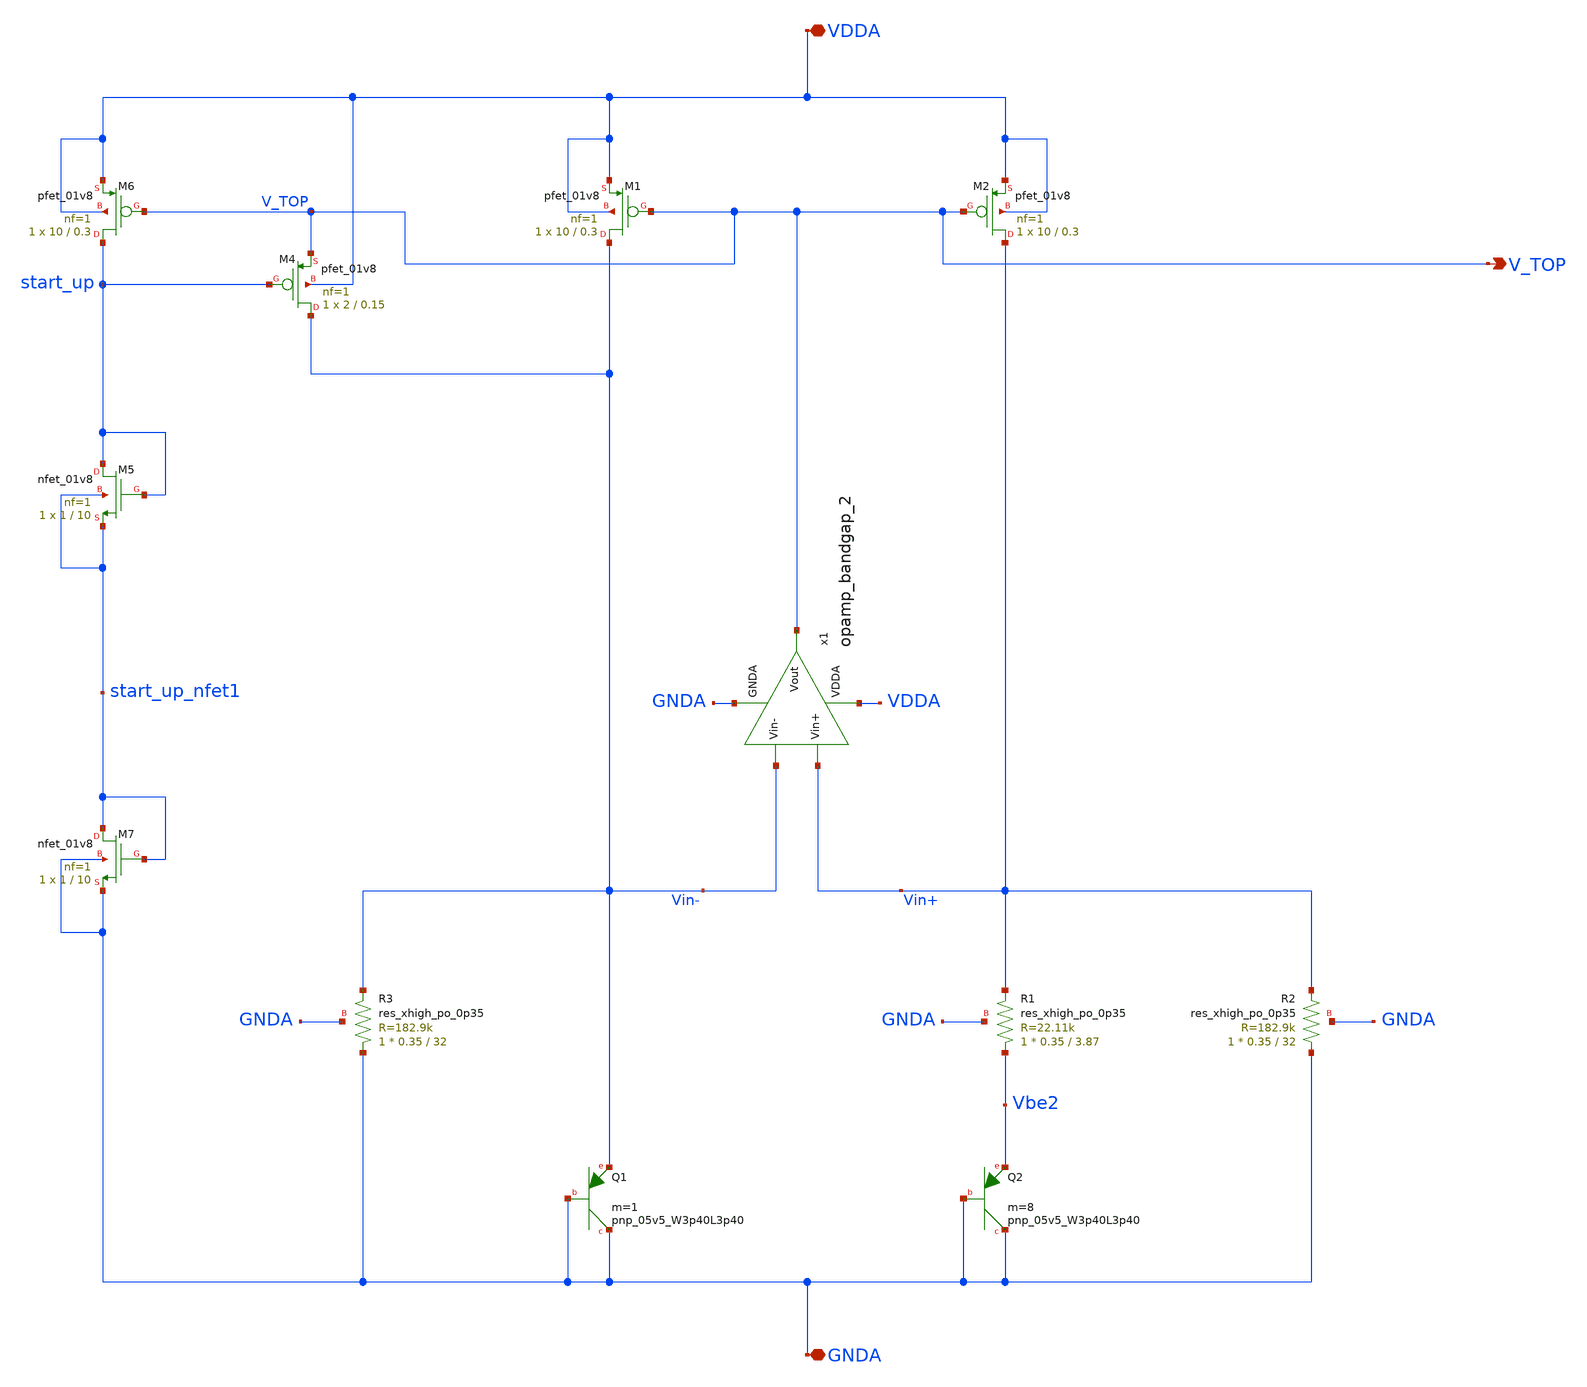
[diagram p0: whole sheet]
** sch_path: projects/bandgapref/xschem_ngspice/new_files/BGR_vtop_out.sch
**.subckt BGR_vtop_out VDDA GNDA V_TOP
*.iopin VDDA
*.iopin GNDA
*.opin V_TOP
XQ1 GNDA GNDA Vin- sky130_fd_pr__pnp_05v5_W3p40L3p40 m=1
XQ2 GNDA GNDA Vbe2 sky130_fd_pr__pnp_05v5_W3p40L3p40 m=8
XM1 Vin- V_TOP VDDA VDDA sky130_fd_pr__pfet_01v8 L=0.3 W=10 nf=1 ad='int((nf+1)/2) * W/nf * 0.29' as='int((nf+2)/2) * W/nf * 0.29'
+ pd='2*int((nf+1)/2) * (W/nf + 0.29)' ps='2*int((nf+2)/2) * (W/nf + 0.29)' nrd='0.29 / W' nrs='0.29 / W'
+ sa=0 sb=0 sd=0 mult=1 m=1
XM2 Vin+ V_TOP VDDA VDDA sky130_fd_pr__pfet_01v8 L=0.3 W=10 nf=1 ad='int((nf+1)/2) * W/nf * 0.29' as='int((nf+2)/2) * W/nf * 0.29'
+ pd='2*int((nf+1)/2) * (W/nf + 0.29)' ps='2*int((nf+2)/2) * (W/nf + 0.29)' nrd='0.29 / W' nrs='0.29 / W'
+ sa=0 sb=0 sd=0 mult=1 m=1
XR1 Vbe2 Vin+ GNDA sky130_fd_pr__res_xhigh_po_0p35 L=3.87 mult=1 m=1
XR2 GNDA Vin+ GNDA sky130_fd_pr__res_xhigh_po_0p35 L=32 mult=1 m=1
XR3 GNDA Vin- GNDA sky130_fd_pr__res_xhigh_po_0p35 L=32 mult=1 m=1
XM5 start_up start_up start_up_nfet1 start_up_nfet1 sky130_fd_pr__nfet_01v8 L=10 W=1 nf=1 ad='int((nf+1)/2) * W/nf * 0.29'
+ as='int((nf+2)/2) * W/nf * 0.29' pd='2*int((nf+1)/2) * (W/nf + 0.29)' ps='2*int((nf+2)/2) * (W/nf + 0.29)'
+ nrd='0.29 / W' nrs='0.29 / W' sa=0 sb=0 sd=0 mult=1 m=1
XM6 start_up V_TOP VDDA VDDA sky130_fd_pr__pfet_01v8 L=0.3 W=10 nf=1 ad='int((nf+1)/2) * W/nf * 0.29'
+ as='int((nf+2)/2) * W/nf * 0.29' pd='2*int((nf+1)/2) * (W/nf + 0.29)' ps='2*int((nf+2)/2) * (W/nf + 0.29)'
+ nrd='0.29 / W' nrs='0.29 / W' sa=0 sb=0 sd=0 mult=1 m=1
XM4 Vin- start_up V_TOP VDDA sky130_fd_pr__pfet_01v8 L=0.15 W=2 nf=1 ad='int((nf+1)/2) * W/nf * 0.29'
+ as='int((nf+2)/2) * W/nf * 0.29' pd='2*int((nf+1)/2) * (W/nf + 0.29)' ps='2*int((nf+2)/2) * (W/nf + 0.29)'
+ nrd='0.29 / W' nrs='0.29 / W' sa=0 sb=0 sd=0 mult=1 m=1
XM7 start_up_nfet1 start_up_nfet1 GNDA GNDA sky130_fd_pr__nfet_01v8 L=10 W=1 nf=1 ad='int((nf+1)/2) * W/nf * 0.29'
+ as='int((nf+2)/2) * W/nf * 0.29' pd='2*int((nf+1)/2) * (W/nf + 0.29)' ps='2*int((nf+2)/2) * (W/nf + 0.29)'
+ nrd='0.29 / W' nrs='0.29 / W' sa=0 sb=0 sd=0 mult=1 m=1
x1 VDDA V_TOP Vin- Vin+ GNDA opamp_bandgap_2
**.ends

* expanding   symbol:
*+  /foss/designs/my_design/projects/bandgapref/xschem_ngspice/new_files/opamp_bandgap_2.sym # of pins=5
** sym_path: projects/bandgapref/xschem_ngspice/new_files/opamp_bandgap_2.sym
** sch_path: projects/bandgapref/xschem_ngspice/new_files/opamp_bandgap_2.sch
.subckt opamp_bandgap_2 VDDA Vout Vin- Vin+ GNDA
*.ipin Vin+
*.opin Vout
*.ipin Vin-
*.ipin GNDA
*.ipin VDDA
XM1 V_p VDDA GNDA GNDA sky130_fd_pr__nfet_01v8 L=5 W=2.5 nf=1 ad='int((nf+1)/2) * W/nf * 0.29' as='int((nf+2)/2) * W/nf * 0.29'
+ pd='2*int((nf+1)/2) * (W/nf + 0.29)' ps='2*int((nf+2)/2) * (W/nf + 0.29)' nrd='0.29 / W' nrs='0.29 / W'
+ sa=0 sb=0 sd=0 mult=1 m=1
XM2 V_mirror Vin- V_p GNDA sky130_fd_pr__nfet_01v8 L=0.2 W=2.5 nf=1 ad='int((nf+1)/2) * W/nf * 0.29'
+ as='int((nf+2)/2) * W/nf * 0.29' pd='2*int((nf+1)/2) * (W/nf + 0.29)' ps='2*int((nf+2)/2) * (W/nf + 0.29)'
+ nrd='0.29 / W' nrs='0.29 / W' sa=0 sb=0 sd=0 mult=1 m=1
XM3 1st_Vout Vin+ V_p GNDA sky130_fd_pr__nfet_01v8 L=0.2 W=2.5 nf=1 ad='int((nf+1)/2) * W/nf * 0.29'
+ as='int((nf+2)/2) * W/nf * 0.29' pd='2*int((nf+1)/2) * (W/nf + 0.29)' ps='2*int((nf+2)/2) * (W/nf + 0.29)'
+ nrd='0.29 / W' nrs='0.29 / W' sa=0 sb=0 sd=0 mult=1 m=1
XM5 V_mirror V_mirror VDDA VDDA sky130_fd_pr__pfet_01v8 L=0.2 W=5 nf=2 ad='int((nf+1)/2) * W/nf * 0.29'
+ as='int((nf+2)/2) * W/nf * 0.29' pd='2*int((nf+1)/2) * (W/nf + 0.29)' ps='2*int((nf+2)/2) * (W/nf + 0.29)'
+ nrd='0.29 / W' nrs='0.29 / W' sa=0 sb=0 sd=0 mult=1 m=1
XM6 1st_Vout V_mirror VDDA VDDA sky130_fd_pr__pfet_01v8 L=0.2 W=5 nf=2 ad='int((nf+1)/2) * W/nf * 0.29'
+ as='int((nf+2)/2) * W/nf * 0.29' pd='2*int((nf+1)/2) * (W/nf + 0.29)' ps='2*int((nf+2)/2) * (W/nf + 0.29)'
+ nrd='0.29 / W' nrs='0.29 / W' sa=0 sb=0 sd=0 mult=1 m=1
XM4 Vout VDDA GNDA GNDA sky130_fd_pr__nfet_01v8 L=5 W=2.5 nf=1 ad='int((nf+1)/2) * W/nf * 0.29' as='int((nf+2)/2) * W/nf * 0.29'
+ pd='2*int((nf+1)/2) * (W/nf + 0.29)' ps='2*int((nf+2)/2) * (W/nf + 0.29)' nrd='0.29 / W' nrs='0.29 / W'
+ sa=0 sb=0 sd=0 mult=1 m=1
XM7 Vout 1st_Vout VDDA VDDA sky130_fd_pr__pfet_01v8 L=0.2 W=5 nf=2 ad='int((nf+1)/2) * W/nf * 0.29' as='int((nf+2)/2) * W/nf * 0.29'
+ pd='2*int((nf+1)/2) * (W/nf + 0.29)' ps='2*int((nf+2)/2) * (W/nf + 0.29)' nrd='0.29 / W' nrs='0.29 / W'
+ sa=0 sb=0 sd=0 mult=1 m=1
XC1 1st_Vout net1 sky130_fd_pr__cap_mim_m3_1 W=10 L=10 MF=1 m=1
XR1 Vout net1 GNDA sky130_fd_pr__res_xhigh_po_0p35 L=4.4 mult=1 m=1
.ends

.end
